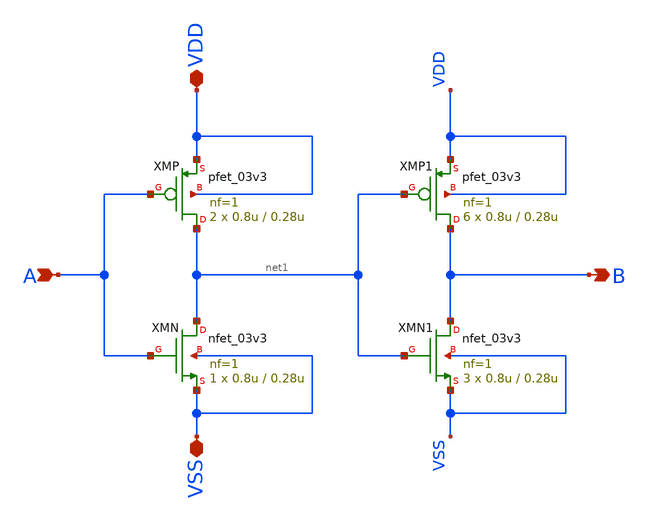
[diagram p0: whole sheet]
** sch_path: designs/gate_buf_x1/gate_buf_x1.sch
**.subckt gate_buf_x1 B A VDD VSS
*.opin B
*.ipin A
*.iopin VDD
*.iopin VSS
XMN net1 A VSS VSS nfet_03v3 L=0.28u W=0.8u nf=1 ad='int((nf+1)/2) * W/nf * 0.18u' as='int((nf+2)/2) * W/nf * 0.18u'
+ pd='2*int((nf+1)/2) * (W/nf + 0.18u)' ps='2*int((nf+2)/2) * (W/nf + 0.18u)' nrd='0.18u / W' nrs='0.18u / W'
+ sa=0 sb=0 sd=0 m=1
XMP net1 A VDD VDD pfet_03v3 L=0.28u W=0.8u nf=1 ad='int((nf+1)/2) * W/nf * 0.18u' as='int((nf+2)/2) * W/nf * 0.18u'
+ pd='2*int((nf+1)/2) * (W/nf + 0.18u)' ps='2*int((nf+2)/2) * (W/nf + 0.18u)' nrd='0.18u / W' nrs='0.18u / W'
+ sa=0 sb=0 sd=0 m=2
XMN1 B net1 VSS VSS nfet_03v3 L=0.28u W=0.8u nf=1 ad='int((nf+1)/2) * W/nf * 0.18u' as='int((nf+2)/2) * W/nf * 0.18u'
+ pd='2*int((nf+1)/2) * (W/nf + 0.18u)' ps='2*int((nf+2)/2) * (W/nf + 0.18u)' nrd='0.18u / W' nrs='0.18u / W'
+ sa=0 sb=0 sd=0 m=3
XMP1 B net1 VDD VDD pfet_03v3 L=0.28u W=0.8u nf=1 ad='int((nf+1)/2) * W/nf * 0.18u' as='int((nf+2)/2) * W/nf * 0.18u'
+ pd='2*int((nf+1)/2) * (W/nf + 0.18u)' ps='2*int((nf+2)/2) * (W/nf + 0.18u)' nrd='0.18u / W' nrs='0.18u / W'
+ sa=0 sb=0 sd=0 m=6
**.ends
.end
